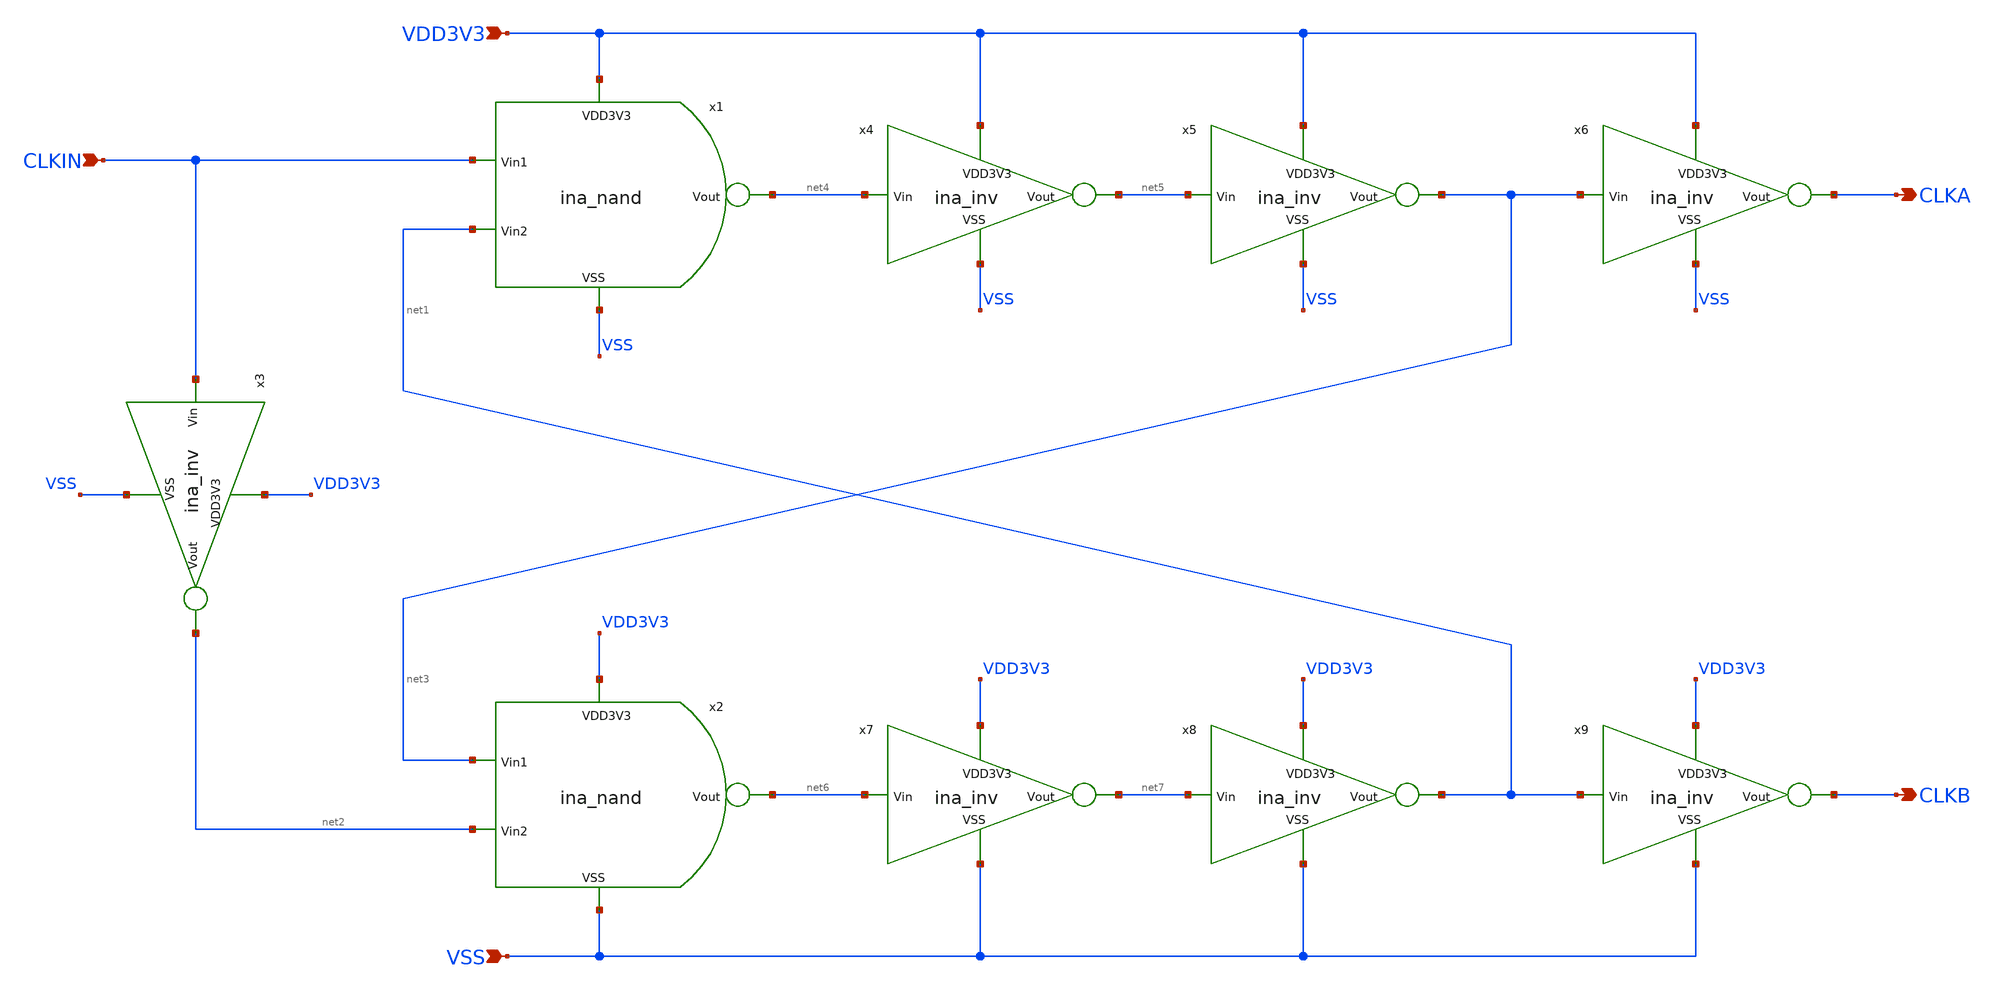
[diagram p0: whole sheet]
** sch_path: designs/libs/core_ina/ina_clockgen/ina_clockgen.sch
**.subckt ina_clockgen CLKIN VDD3V3 VSS CLKA CLKB
*.ipin CLKIN
*.ipin VDD3V3
*.ipin VSS
*.opin CLKA
*.opin CLKB
x1 VDD3V3 net4 CLKIN net1 VSS ina_nand
x2 VDD3V3 net6 net3 net2 VSS ina_nand
x3 VDD3V3 CLKIN net2 VSS ina_inv
x4 VDD3V3 net4 net5 VSS ina_inv
x5 VDD3V3 net5 net3 VSS ina_inv
x6 VDD3V3 net3 CLKA VSS ina_inv
x7 VDD3V3 net6 net7 VSS ina_inv
x8 VDD3V3 net7 net1 VSS ina_inv
x9 VDD3V3 net1 CLKB VSS ina_inv
**.ends

* expanding   symbol:  /foss/designs/core_ina/ina_nand.sym # of pins=5
** sym_path: designs/libs/core_ina/ina_nand/ina_nand.sym
** sch_path: designs/libs/core_ina/ina_nand/ina_nand.sch
.subckt ina_nand VDD3V3 Vout Vin1 Vin2 VSS
*.ipin VDD3V3
*.ipin Vin1
*.ipin Vin2
*.ipin VSS
*.opin Vout
XMN1 Vout Vin1 VDD3V3 VDD3V3 pfet_03v3 L=0.28u W=2u nf=1 ad='int((nf+1)/2) * W/nf * 0.18u' as='int((nf+2)/2) * W/nf * 0.18u'
+ pd='2*int((nf+1)/2) * (W/nf + 0.18u)' ps='2*int((nf+2)/2) * (W/nf + 0.18u)' nrd='0.18u / W' nrs='0.18u / W'
+ sa=0 sb=0 sd=0 m=1
XMN2 Vout Vin2 VDD3V3 VDD3V3 pfet_03v3 L=0.28u W=2u nf=1 ad='int((nf+1)/2) * W/nf * 0.18u' as='int((nf+2)/2) * W/nf * 0.18u'
+ pd='2*int((nf+1)/2) * (W/nf + 0.18u)' ps='2*int((nf+2)/2) * (W/nf + 0.18u)' nrd='0.18u / W' nrs='0.18u / W'
+ sa=0 sb=0 sd=0 m=1
XMN3 Vout Vin1 net1 VSS nfet_03v3 L=0.28u W=2u nf=1 ad='int((nf+1)/2) * W/nf * 0.18u' as='int((nf+2)/2) * W/nf * 0.18u'
+ pd='2*int((nf+1)/2) * (W/nf + 0.18u)' ps='2*int((nf+2)/2) * (W/nf + 0.18u)' nrd='0.18u / W' nrs='0.18u / W'
+ sa=0 sb=0 sd=0 m=1
XMN4 net1 Vin2 VSS VSS nfet_03v3 L=0.28u W=2u nf=1 ad='int((nf+1)/2) * W/nf * 0.18u' as='int((nf+2)/2) * W/nf * 0.18u'
+ pd='2*int((nf+1)/2) * (W/nf + 0.18u)' ps='2*int((nf+2)/2) * (W/nf + 0.18u)' nrd='0.18u / W' nrs='0.18u / W'
+ sa=0 sb=0 sd=0 m=1
.ends


* expanding   symbol:  /foss/designs/core_ina/ina_inv.sym # of pins=4
** sym_path: designs/libs/core_ina/ina_inv/ina_inv.sym
** sch_path: designs/libs/core_ina/ina_inv/ina_inv.sch
.subckt ina_inv VDD3V3 Vin Vout VSS
*.ipin VDD3V3
*.ipin VSS
*.ipin Vin
*.opin Vout
XMI1 Vout Vin VDD3V3 VDD3V3 pfet_03v3 L=0.28u W=2u nf=1 ad='int((nf+1)/2) * W/nf * 0.18u' as='int((nf+2)/2) * W/nf * 0.18u'
+ pd='2*int((nf+1)/2) * (W/nf + 0.18u)' ps='2*int((nf+2)/2) * (W/nf + 0.18u)' nrd='0.18u / W' nrs='0.18u / W'
+ sa=0 sb=0 sd=0 m=1
XMI2 Vout Vin VSS VSS nfet_03v3 L=0.28u W=1u nf=1 ad='int((nf+1)/2) * W/nf * 0.18u' as='int((nf+2)/2) * W/nf * 0.18u'
+ pd='2*int((nf+1)/2) * (W/nf + 0.18u)' ps='2*int((nf+2)/2) * (W/nf + 0.18u)' nrd='0.18u / W' nrs='0.18u / W'
+ sa=0 sb=0 sd=0 m=1
.ends

.end
